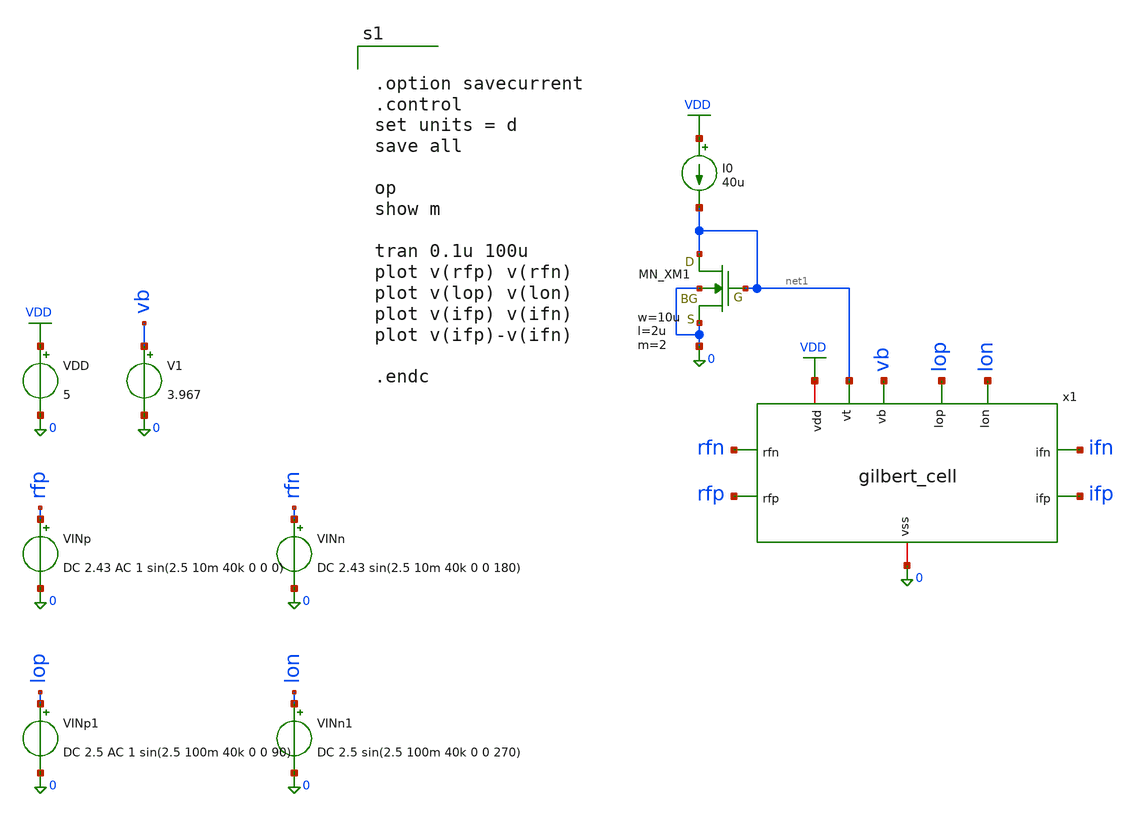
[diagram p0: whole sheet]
** sch_path: member_project/JJY_Receiver/Masahiro/jjy_recv/gilbert_cell/gilbert_cell_sim.sch
**.subckt gilbert_cell_sim
VDD VDD 0 5
VINp rfp 0 DC 2.43 AC 1 sin(2.5 10m 40k 0 0 0)
V1 vb 0 3.967
VINn rfn 0 DC 2.43 sin(2.5 10m 40k 0 0 180)
I0 VDD net1 40u
VINp1 lop 0 DC 2.5 AC 1 sin(2.5 100m 40k 0 0 90)
VINn1 lon 0 DC 2.5 sin(2.5 100m 40k 0 0 270)
XXM1 net1 net1 0 0 NMOS w=10u l=2u nrd=0 nrs=0 m=2
x1 vb ifn VDD ifp 0 lop lon rfn rfp net1 gilbert_cell
**** begin user architecture code
 .include $::LIB/ip62_models


.option savecurrent
.control
set units = d
save all

op
show m

tran 0.1u 100u
plot v(rfp) v(rfn)
plot v(lop) v(lon)
plot v(ifp) v(ifn)
plot v(ifp)-v(ifn)

.endc


**** end user architecture code
**.ends

* expanding   symbol:
*+  /home/ishi-kai/ISHI-KAI_Multiple_Projects_OpenMPW_OpenSUSI-TR10-1/member_project/JJY_Receiver/Masahiro/jjy_recv/gilbert_cell/gilbert_cell.sym # of pins=10
** sym_path: member_project/JJY_Receiver/Masahiro/jjy_recv/gilbert_cell/gilbert_cell.sym
** sch_path: member_project/JJY_Receiver/Masahiro/jjy_recv/gilbert_cell/gilbert_cell.sch
.subckt gilbert_cell vb ifn vdd ifp vss lop lon rfn rfp vt
*.opin ifp
*.opin ifn
*.ipin rfp
*.ipin vb
*.ipin vt
*.ipin rfn
*.iopin vdd
*.iopin vss
*.ipin lon
*.ipin lop
XM1 ifp vb vdd vdd PMOS w=45u l=2u as=0 ad=0 ps=0 pd=0 nrd=0 nrs=0 m=1
XM2 ifn vb vdd vdd PMOS w=45u l=2u as=0 ad=0 ps=0 pd=0 nrd=0 nrs=0 m=1
XM3 net3 vt vss vss NMOS w=10u l=2u as=0 ad=0 ps=0 pd=0 nrd=0 nrs=0 m=2
XM7 net1 rfp net3 vss NMOS w=20u l=2u as=0 ad=0 ps=0 pd=0 nrd=0 nrs=0 m=1
XM8 net2 rfn net3 vss NMOS w=20u l=2u as=0 ad=0 ps=0 pd=0 nrd=0 nrs=0 m=1
XM5 ifn lop net1 vss NMOS w=20u l=2u as=0 ad=0 ps=0 pd=0 nrd=0 nrs=0 m=1
XM6 ifp lon net1 vss NMOS w=20u l=2u as=0 ad=0 ps=0 pd=0 nrd=0 nrs=0 m=1
XM9 ifn lon net2 vss NMOS w=20u l=2u as=0 ad=0 ps=0 pd=0 nrd=0 nrs=0 m=1
XM10 ifp lop net2 vss NMOS w=20u l=2u as=0 ad=0 ps=0 pd=0 nrd=0 nrs=0 m=1
.ends

.GLOBAL VDD
.end
